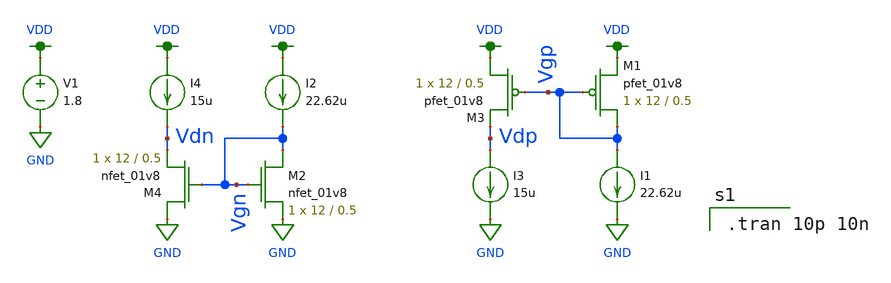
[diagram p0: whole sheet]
** sch_path: mp3/xschem/test_pmos.sch
**.subckt test_pmos
XM1 Vgp Vgp VDD VDD sky130_fd_pr__pfet_01v8 L=0.5 W=12 nf=1 ad='int((nf+1)/2) * W/nf * 0.29' as='int((nf+2)/2) * W/nf * 0.29'
+ pd='2*int((nf+1)/2) * (W/nf + 0.29)' ps='2*int((nf+2)/2) * (W/nf + 0.29)' nrd='0.29 / W' nrs='0.29 / W'
+ sa=0 sb=0 sd=0 mult=1 m=1
V1 VDD GND 1.8
I1 Vgp GND 22.62u
XM2 Vgn Vgn GND GND sky130_fd_pr__nfet_01v8 L=0.5 W=12 nf=1 ad='int((nf+1)/2) * W/nf * 0.29' as='int((nf+2)/2) * W/nf * 0.29'
+ pd='2*int((nf+1)/2) * (W/nf + 0.29)' ps='2*int((nf+2)/2) * (W/nf + 0.29)' nrd='0.29 / W' nrs='0.29 / W'
+ sa=0 sb=0 sd=0 mult=1 m=1
I2 VDD Vgn 22.62u
XM3 VDD Vgp Vdp VDD sky130_fd_pr__pfet_01v8 L=0.5 W=12 nf=1 ad='int((nf+1)/2) * W/nf * 0.29' as='int((nf+2)/2) * W/nf * 0.29'
+ pd='2*int((nf+1)/2) * (W/nf + 0.29)' ps='2*int((nf+2)/2) * (W/nf + 0.29)' nrd='0.29 / W' nrs='0.29 / W'
+ sa=0 sb=0 sd=0 mult=1 m=1
XM4 GND Vgn Vdn GND sky130_fd_pr__nfet_01v8 L=0.5 W=12 nf=1 ad='int((nf+1)/2) * W/nf * 0.29' as='int((nf+2)/2) * W/nf * 0.29'
+ pd='2*int((nf+1)/2) * (W/nf + 0.29)' ps='2*int((nf+2)/2) * (W/nf + 0.29)' nrd='0.29 / W' nrs='0.29 / W'
+ sa=0 sb=0 sd=0 mult=1 m=1
I3 Vdp GND 15u
I4 VDD Vdn 15u
**** begin user architecture code

.option wnflag=1
.lib ~/skywater/skywater-pdk/libraries/sky130_fd_pr_ngspice/latest/models/sky130.lib.spice tt


.tran 10p 10n

**** end user architecture code
**.ends
.GLOBAL VDD
.GLOBAL GND
.end
